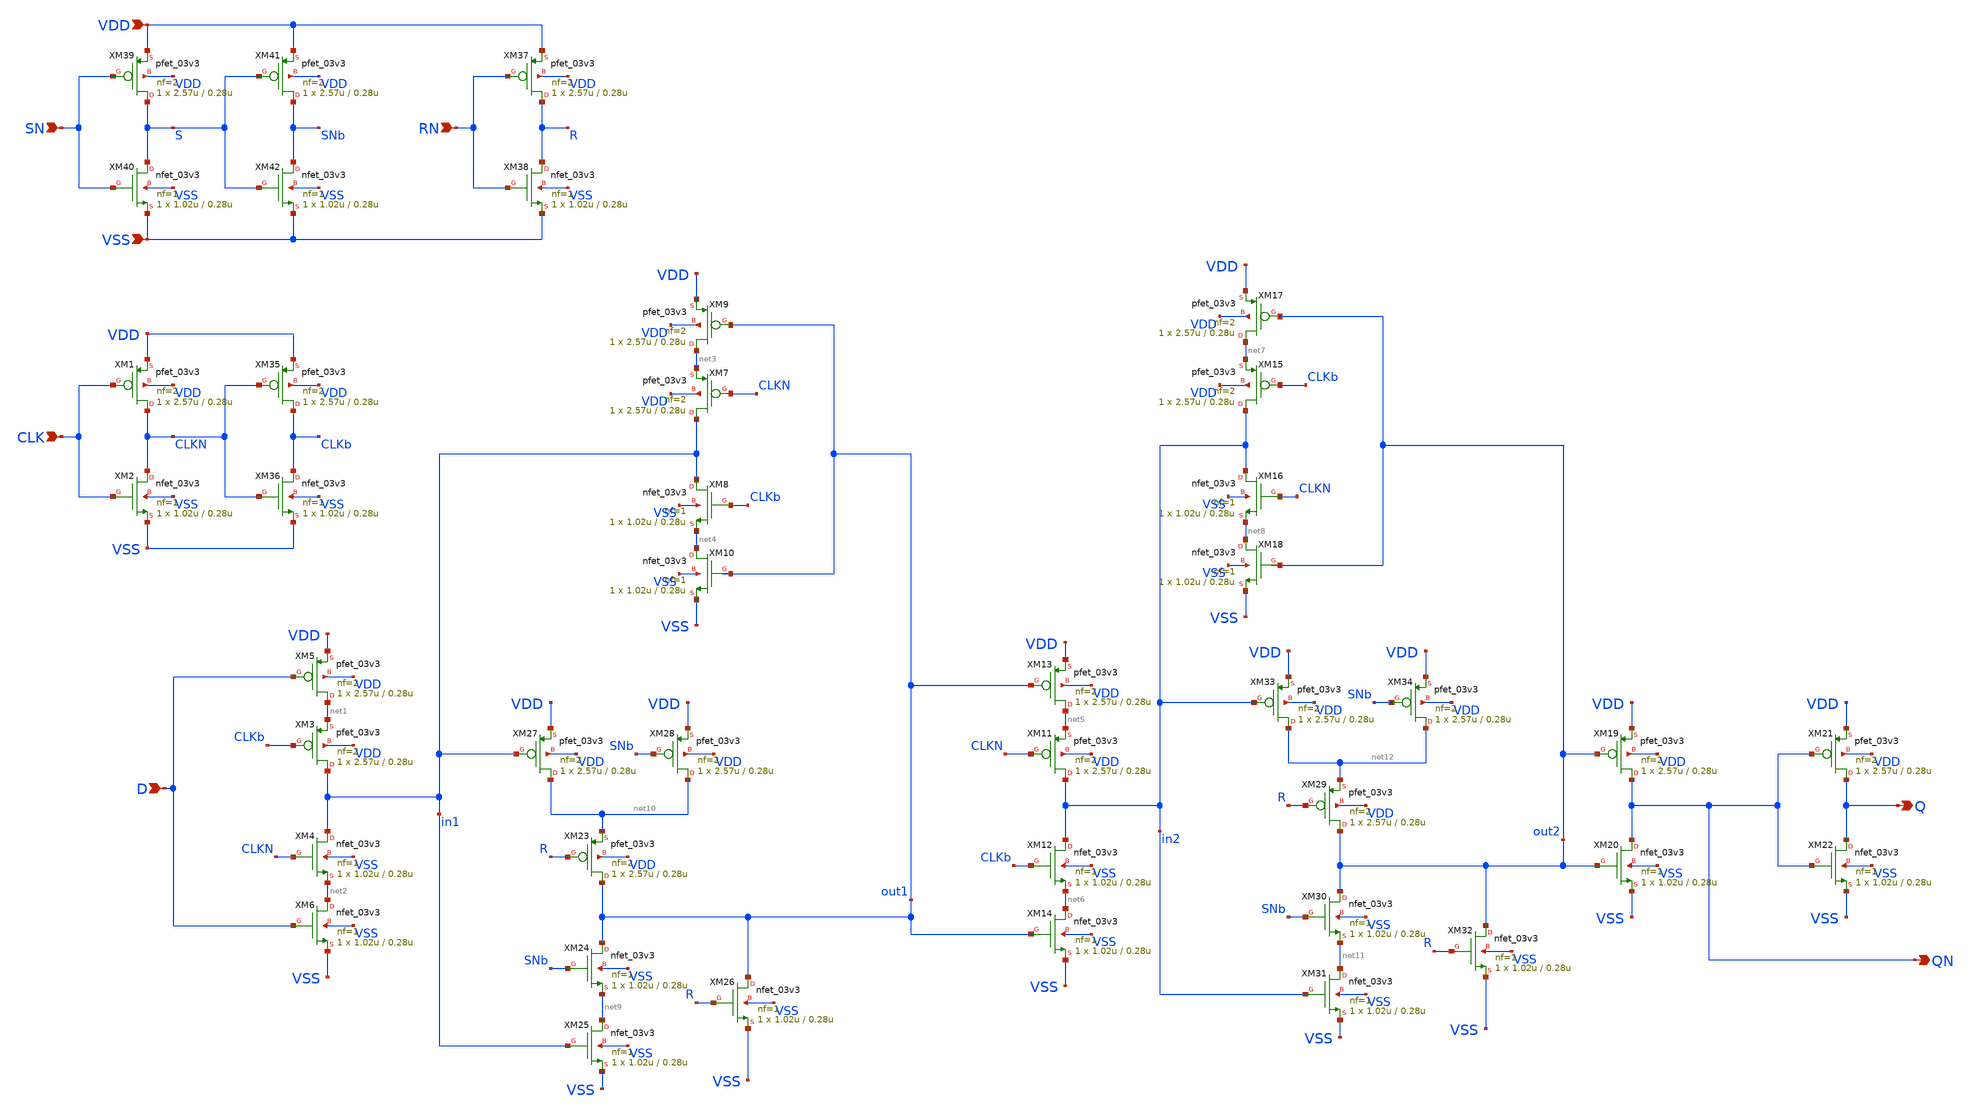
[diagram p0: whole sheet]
** sch_path: xschem/gf180mcu_ocd_sc_rt12t3v3__dffsr_1.sch
**.subckt gf180mcu_ocd_sc_rt12t3v3__dffsr_1 D CLK SN RN Q QN VDD VSS
*.ipin D
*.ipin CLK
*.ipin SN
*.ipin RN
*.opin Q
*.opin QN
*.ipin VDD
*.ipin VSS
XM1 CLKN CLK VDD VDD pfet_03v3 L=0.28u W=2.57u nf=2 ad='int((nf+1)/2) * W/nf * 0.18u' as='int((nf+2)/2) * W/nf * 0.18u'
+ pd='2*int((nf+1)/2) * (W/nf + 0.18u)' ps='2*int((nf+2)/2) * (W/nf + 0.18u)' nrd='0.18u / W' nrs='0.18u / W'
+ sa=0 sb=0 sd=0 m=1
XM2 CLKN CLK VSS VSS nfet_03v3 L=0.28u W=1.02u nf=1 ad='int((nf+1)/2) * W/nf * 0.18u' as='int((nf+2)/2) * W/nf * 0.18u'
+ pd='2*int((nf+1)/2) * (W/nf + 0.18u)' ps='2*int((nf+2)/2) * (W/nf + 0.18u)' nrd='0.18u / W' nrs='0.18u / W'
+ sa=0 sb=0 sd=0 m=1
XM3 in1 CLKb net1 VDD pfet_03v3 L=0.28u W=2.57u nf=2 ad='int((nf+1)/2) * W/nf * 0.18u' as='int((nf+2)/2) * W/nf * 0.18u'
+ pd='2*int((nf+1)/2) * (W/nf + 0.18u)' ps='2*int((nf+2)/2) * (W/nf + 0.18u)' nrd='0.18u / W' nrs='0.18u / W'
+ sa=0 sb=0 sd=0 m=1
XM4 in1 CLKN net2 VSS nfet_03v3 L=0.28u W=1.02u nf=1 ad='int((nf+1)/2) * W/nf * 0.18u' as='int((nf+2)/2) * W/nf * 0.18u'
+ pd='2*int((nf+1)/2) * (W/nf + 0.18u)' ps='2*int((nf+2)/2) * (W/nf + 0.18u)' nrd='0.18u / W' nrs='0.18u / W'
+ sa=0 sb=0 sd=0 m=1
XM5 net1 D VDD VDD pfet_03v3 L=0.28u W=2.57u nf=2 ad='int((nf+1)/2) * W/nf * 0.18u' as='int((nf+2)/2) * W/nf * 0.18u'
+ pd='2*int((nf+1)/2) * (W/nf + 0.18u)' ps='2*int((nf+2)/2) * (W/nf + 0.18u)' nrd='0.18u / W' nrs='0.18u / W'
+ sa=0 sb=0 sd=0 m=1
XM6 net2 D VSS VSS nfet_03v3 L=0.28u W=1.02u nf=1 ad='int((nf+1)/2) * W/nf * 0.18u' as='int((nf+2)/2) * W/nf * 0.18u'
+ pd='2*int((nf+1)/2) * (W/nf + 0.18u)' ps='2*int((nf+2)/2) * (W/nf + 0.18u)' nrd='0.18u / W' nrs='0.18u / W'
+ sa=0 sb=0 sd=0 m=1
XM7 in1 CLKN net3 VDD pfet_03v3 L=0.28u W=2.57u nf=2 ad='int((nf+1)/2) * W/nf * 0.18u' as='int((nf+2)/2) * W/nf * 0.18u'
+ pd='2*int((nf+1)/2) * (W/nf + 0.18u)' ps='2*int((nf+2)/2) * (W/nf + 0.18u)' nrd='0.18u / W' nrs='0.18u / W'
+ sa=0 sb=0 sd=0 m=1
XM8 in1 CLKb net4 VSS nfet_03v3 L=0.28u W=1.02u nf=1 ad='int((nf+1)/2) * W/nf * 0.18u' as='int((nf+2)/2) * W/nf * 0.18u'
+ pd='2*int((nf+1)/2) * (W/nf + 0.18u)' ps='2*int((nf+2)/2) * (W/nf + 0.18u)' nrd='0.18u / W' nrs='0.18u / W'
+ sa=0 sb=0 sd=0 m=1
XM9 net3 out1 VDD VDD pfet_03v3 L=0.28u W=2.57u nf=2 ad='int((nf+1)/2) * W/nf * 0.18u' as='int((nf+2)/2) * W/nf * 0.18u'
+ pd='2*int((nf+1)/2) * (W/nf + 0.18u)' ps='2*int((nf+2)/2) * (W/nf + 0.18u)' nrd='0.18u / W' nrs='0.18u / W'
+ sa=0 sb=0 sd=0 m=1
XM10 net4 out1 VSS VSS nfet_03v3 L=0.28u W=1.02u nf=1 ad='int((nf+1)/2) * W/nf * 0.18u' as='int((nf+2)/2) * W/nf * 0.18u'
+ pd='2*int((nf+1)/2) * (W/nf + 0.18u)' ps='2*int((nf+2)/2) * (W/nf + 0.18u)' nrd='0.18u / W' nrs='0.18u / W'
+ sa=0 sb=0 sd=0 m=1
XM11 in2 CLKN net5 VDD pfet_03v3 L=0.28u W=2.57u nf=2 ad='int((nf+1)/2) * W/nf * 0.18u' as='int((nf+2)/2) * W/nf * 0.18u'
+ pd='2*int((nf+1)/2) * (W/nf + 0.18u)' ps='2*int((nf+2)/2) * (W/nf + 0.18u)' nrd='0.18u / W' nrs='0.18u / W'
+ sa=0 sb=0 sd=0 m=1
XM12 in2 CLKb net6 VSS nfet_03v3 L=0.28u W=1.02u nf=1 ad='int((nf+1)/2) * W/nf * 0.18u' as='int((nf+2)/2) * W/nf * 0.18u'
+ pd='2*int((nf+1)/2) * (W/nf + 0.18u)' ps='2*int((nf+2)/2) * (W/nf + 0.18u)' nrd='0.18u / W' nrs='0.18u / W'
+ sa=0 sb=0 sd=0 m=1
XM13 net5 out1 VDD VDD pfet_03v3 L=0.28u W=2.57u nf=2 ad='int((nf+1)/2) * W/nf * 0.18u' as='int((nf+2)/2) * W/nf * 0.18u'
+ pd='2*int((nf+1)/2) * (W/nf + 0.18u)' ps='2*int((nf+2)/2) * (W/nf + 0.18u)' nrd='0.18u / W' nrs='0.18u / W'
+ sa=0 sb=0 sd=0 m=1
XM14 net6 out1 VSS VSS nfet_03v3 L=0.28u W=1.02u nf=1 ad='int((nf+1)/2) * W/nf * 0.18u' as='int((nf+2)/2) * W/nf * 0.18u'
+ pd='2*int((nf+1)/2) * (W/nf + 0.18u)' ps='2*int((nf+2)/2) * (W/nf + 0.18u)' nrd='0.18u / W' nrs='0.18u / W'
+ sa=0 sb=0 sd=0 m=1
XM15 in2 CLKb net7 VDD pfet_03v3 L=0.28u W=2.57u nf=2 ad='int((nf+1)/2) * W/nf * 0.18u' as='int((nf+2)/2) * W/nf * 0.18u'
+ pd='2*int((nf+1)/2) * (W/nf + 0.18u)' ps='2*int((nf+2)/2) * (W/nf + 0.18u)' nrd='0.18u / W' nrs='0.18u / W'
+ sa=0 sb=0 sd=0 m=1
XM16 in2 CLKN net8 VSS nfet_03v3 L=0.28u W=1.02u nf=1 ad='int((nf+1)/2) * W/nf * 0.18u' as='int((nf+2)/2) * W/nf * 0.18u'
+ pd='2*int((nf+1)/2) * (W/nf + 0.18u)' ps='2*int((nf+2)/2) * (W/nf + 0.18u)' nrd='0.18u / W' nrs='0.18u / W'
+ sa=0 sb=0 sd=0 m=1
XM17 net7 out2 VDD VDD pfet_03v3 L=0.28u W=2.57u nf=2 ad='int((nf+1)/2) * W/nf * 0.18u' as='int((nf+2)/2) * W/nf * 0.18u'
+ pd='2*int((nf+1)/2) * (W/nf + 0.18u)' ps='2*int((nf+2)/2) * (W/nf + 0.18u)' nrd='0.18u / W' nrs='0.18u / W'
+ sa=0 sb=0 sd=0 m=1
XM18 net8 out2 VSS VSS nfet_03v3 L=0.28u W=1.02u nf=1 ad='int((nf+1)/2) * W/nf * 0.18u' as='int((nf+2)/2) * W/nf * 0.18u'
+ pd='2*int((nf+1)/2) * (W/nf + 0.18u)' ps='2*int((nf+2)/2) * (W/nf + 0.18u)' nrd='0.18u / W' nrs='0.18u / W'
+ sa=0 sb=0 sd=0 m=1
XM19 QN out2 VDD VDD pfet_03v3 L=0.28u W=2.57u nf=2 ad='int((nf+1)/2) * W/nf * 0.18u' as='int((nf+2)/2) * W/nf * 0.18u'
+ pd='2*int((nf+1)/2) * (W/nf + 0.18u)' ps='2*int((nf+2)/2) * (W/nf + 0.18u)' nrd='0.18u / W' nrs='0.18u / W'
+ sa=0 sb=0 sd=0 m=1
XM20 QN out2 VSS VSS nfet_03v3 L=0.28u W=1.02u nf=1 ad='int((nf+1)/2) * W/nf * 0.18u' as='int((nf+2)/2) * W/nf * 0.18u'
+ pd='2*int((nf+1)/2) * (W/nf + 0.18u)' ps='2*int((nf+2)/2) * (W/nf + 0.18u)' nrd='0.18u / W' nrs='0.18u / W'
+ sa=0 sb=0 sd=0 m=1
XM21 Q QN VDD VDD pfet_03v3 L=0.28u W=2.57u nf=2 ad='int((nf+1)/2) * W/nf * 0.18u' as='int((nf+2)/2) * W/nf * 0.18u'
+ pd='2*int((nf+1)/2) * (W/nf + 0.18u)' ps='2*int((nf+2)/2) * (W/nf + 0.18u)' nrd='0.18u / W' nrs='0.18u / W'
+ sa=0 sb=0 sd=0 m=1
XM22 Q QN VSS VSS nfet_03v3 L=0.28u W=1.02u nf=1 ad='int((nf+1)/2) * W/nf * 0.18u' as='int((nf+2)/2) * W/nf * 0.18u'
+ pd='2*int((nf+1)/2) * (W/nf + 0.18u)' ps='2*int((nf+2)/2) * (W/nf + 0.18u)' nrd='0.18u / W' nrs='0.18u / W'
+ sa=0 sb=0 sd=0 m=1
XM23 out1 R net10 VDD pfet_03v3 L=0.28u W=2.57u nf=2 ad='int((nf+1)/2) * W/nf * 0.18u' as='int((nf+2)/2) * W/nf * 0.18u'
+ pd='2*int((nf+1)/2) * (W/nf + 0.18u)' ps='2*int((nf+2)/2) * (W/nf + 0.18u)' nrd='0.18u / W' nrs='0.18u / W'
+ sa=0 sb=0 sd=0 m=1
XM24 out1 SNb net9 VSS nfet_03v3 L=0.28u W=1.02u nf=1 ad='int((nf+1)/2) * W/nf * 0.18u' as='int((nf+2)/2) * W/nf * 0.18u'
+ pd='2*int((nf+1)/2) * (W/nf + 0.18u)' ps='2*int((nf+2)/2) * (W/nf + 0.18u)' nrd='0.18u / W' nrs='0.18u / W'
+ sa=0 sb=0 sd=0 m=1
XM25 net9 in1 VSS VSS nfet_03v3 L=0.28u W=1.02u nf=1 ad='int((nf+1)/2) * W/nf * 0.18u' as='int((nf+2)/2) * W/nf * 0.18u'
+ pd='2*int((nf+1)/2) * (W/nf + 0.18u)' ps='2*int((nf+2)/2) * (W/nf + 0.18u)' nrd='0.18u / W' nrs='0.18u / W'
+ sa=0 sb=0 sd=0 m=1
XM26 out1 R VSS VSS nfet_03v3 L=0.28u W=1.02u nf=1 ad='int((nf+1)/2) * W/nf * 0.18u' as='int((nf+2)/2) * W/nf * 0.18u'
+ pd='2*int((nf+1)/2) * (W/nf + 0.18u)' ps='2*int((nf+2)/2) * (W/nf + 0.18u)' nrd='0.18u / W' nrs='0.18u / W'
+ sa=0 sb=0 sd=0 m=1
XM27 net10 in1 VDD VDD pfet_03v3 L=0.28u W=2.57u nf=2 ad='int((nf+1)/2) * W/nf * 0.18u' as='int((nf+2)/2) * W/nf * 0.18u'
+ pd='2*int((nf+1)/2) * (W/nf + 0.18u)' ps='2*int((nf+2)/2) * (W/nf + 0.18u)' nrd='0.18u / W' nrs='0.18u / W'
+ sa=0 sb=0 sd=0 m=1
XM28 net10 SNb VDD VDD pfet_03v3 L=0.28u W=2.57u nf=2 ad='int((nf+1)/2) * W/nf * 0.18u' as='int((nf+2)/2) * W/nf * 0.18u'
+ pd='2*int((nf+1)/2) * (W/nf + 0.18u)' ps='2*int((nf+2)/2) * (W/nf + 0.18u)' nrd='0.18u / W' nrs='0.18u / W'
+ sa=0 sb=0 sd=0 m=1
XM29 out2 R net12 VDD pfet_03v3 L=0.28u W=2.57u nf=2 ad='int((nf+1)/2) * W/nf * 0.18u' as='int((nf+2)/2) * W/nf * 0.18u'
+ pd='2*int((nf+1)/2) * (W/nf + 0.18u)' ps='2*int((nf+2)/2) * (W/nf + 0.18u)' nrd='0.18u / W' nrs='0.18u / W'
+ sa=0 sb=0 sd=0 m=1
XM30 out2 SNb net11 VSS nfet_03v3 L=0.28u W=1.02u nf=1 ad='int((nf+1)/2) * W/nf * 0.18u' as='int((nf+2)/2) * W/nf * 0.18u'
+ pd='2*int((nf+1)/2) * (W/nf + 0.18u)' ps='2*int((nf+2)/2) * (W/nf + 0.18u)' nrd='0.18u / W' nrs='0.18u / W'
+ sa=0 sb=0 sd=0 m=1
XM31 net11 in2 VSS VSS nfet_03v3 L=0.28u W=1.02u nf=1 ad='int((nf+1)/2) * W/nf * 0.18u' as='int((nf+2)/2) * W/nf * 0.18u'
+ pd='2*int((nf+1)/2) * (W/nf + 0.18u)' ps='2*int((nf+2)/2) * (W/nf + 0.18u)' nrd='0.18u / W' nrs='0.18u / W'
+ sa=0 sb=0 sd=0 m=1
XM32 out2 R VSS VSS nfet_03v3 L=0.28u W=1.02u nf=1 ad='int((nf+1)/2) * W/nf * 0.18u' as='int((nf+2)/2) * W/nf * 0.18u'
+ pd='2*int((nf+1)/2) * (W/nf + 0.18u)' ps='2*int((nf+2)/2) * (W/nf + 0.18u)' nrd='0.18u / W' nrs='0.18u / W'
+ sa=0 sb=0 sd=0 m=1
XM33 net12 in2 VDD VDD pfet_03v3 L=0.28u W=2.57u nf=2 ad='int((nf+1)/2) * W/nf * 0.18u' as='int((nf+2)/2) * W/nf * 0.18u'
+ pd='2*int((nf+1)/2) * (W/nf + 0.18u)' ps='2*int((nf+2)/2) * (W/nf + 0.18u)' nrd='0.18u / W' nrs='0.18u / W'
+ sa=0 sb=0 sd=0 m=1
XM34 net12 SNb VDD VDD pfet_03v3 L=0.28u W=2.57u nf=2 ad='int((nf+1)/2) * W/nf * 0.18u' as='int((nf+2)/2) * W/nf * 0.18u'
+ pd='2*int((nf+1)/2) * (W/nf + 0.18u)' ps='2*int((nf+2)/2) * (W/nf + 0.18u)' nrd='0.18u / W' nrs='0.18u / W'
+ sa=0 sb=0 sd=0 m=1
XM37 R RN VDD VDD pfet_03v3 L=0.28u W=2.57u nf=2 ad='int((nf+1)/2) * W/nf * 0.18u' as='int((nf+2)/2) * W/nf * 0.18u'
+ pd='2*int((nf+1)/2) * (W/nf + 0.18u)' ps='2*int((nf+2)/2) * (W/nf + 0.18u)' nrd='0.18u / W' nrs='0.18u / W'
+ sa=0 sb=0 sd=0 m=1
XM38 R RN VSS VSS nfet_03v3 L=0.28u W=1.02u nf=1 ad='int((nf+1)/2) * W/nf * 0.18u' as='int((nf+2)/2) * W/nf * 0.18u'
+ pd='2*int((nf+1)/2) * (W/nf + 0.18u)' ps='2*int((nf+2)/2) * (W/nf + 0.18u)' nrd='0.18u / W' nrs='0.18u / W'
+ sa=0 sb=0 sd=0 m=1
XM35 CLKb CLKN VDD VDD pfet_03v3 L=0.28u W=2.57u nf=2 ad='int((nf+1)/2) * W/nf * 0.18u' as='int((nf+2)/2) * W/nf * 0.18u'
+ pd='2*int((nf+1)/2) * (W/nf + 0.18u)' ps='2*int((nf+2)/2) * (W/nf + 0.18u)' nrd='0.18u / W' nrs='0.18u / W'
+ sa=0 sb=0 sd=0 m=1
XM36 CLKb CLKN VSS VSS nfet_03v3 L=0.28u W=1.02u nf=1 ad='int((nf+1)/2) * W/nf * 0.18u' as='int((nf+2)/2) * W/nf * 0.18u'
+ pd='2*int((nf+1)/2) * (W/nf + 0.18u)' ps='2*int((nf+2)/2) * (W/nf + 0.18u)' nrd='0.18u / W' nrs='0.18u / W'
+ sa=0 sb=0 sd=0 m=1
XM39 S SN VDD VDD pfet_03v3 L=0.28u W=2.57u nf=2 ad='int((nf+1)/2) * W/nf * 0.18u' as='int((nf+2)/2) * W/nf * 0.18u'
+ pd='2*int((nf+1)/2) * (W/nf + 0.18u)' ps='2*int((nf+2)/2) * (W/nf + 0.18u)' nrd='0.18u / W' nrs='0.18u / W'
+ sa=0 sb=0 sd=0 m=1
XM40 S SN VSS VSS nfet_03v3 L=0.28u W=1.02u nf=1 ad='int((nf+1)/2) * W/nf * 0.18u' as='int((nf+2)/2) * W/nf * 0.18u'
+ pd='2*int((nf+1)/2) * (W/nf + 0.18u)' ps='2*int((nf+2)/2) * (W/nf + 0.18u)' nrd='0.18u / W' nrs='0.18u / W'
+ sa=0 sb=0 sd=0 m=1
XM41 SNb S VDD VDD pfet_03v3 L=0.28u W=2.57u nf=2 ad='int((nf+1)/2) * W/nf * 0.18u' as='int((nf+2)/2) * W/nf * 0.18u'
+ pd='2*int((nf+1)/2) * (W/nf + 0.18u)' ps='2*int((nf+2)/2) * (W/nf + 0.18u)' nrd='0.18u / W' nrs='0.18u / W'
+ sa=0 sb=0 sd=0 m=1
XM42 SNb S VSS VSS nfet_03v3 L=0.28u W=1.02u nf=1 ad='int((nf+1)/2) * W/nf * 0.18u' as='int((nf+2)/2) * W/nf * 0.18u'
+ pd='2*int((nf+1)/2) * (W/nf + 0.18u)' ps='2*int((nf+2)/2) * (W/nf + 0.18u)' nrd='0.18u / W' nrs='0.18u / W'
+ sa=0 sb=0 sd=0 m=1
**.ends
.end
